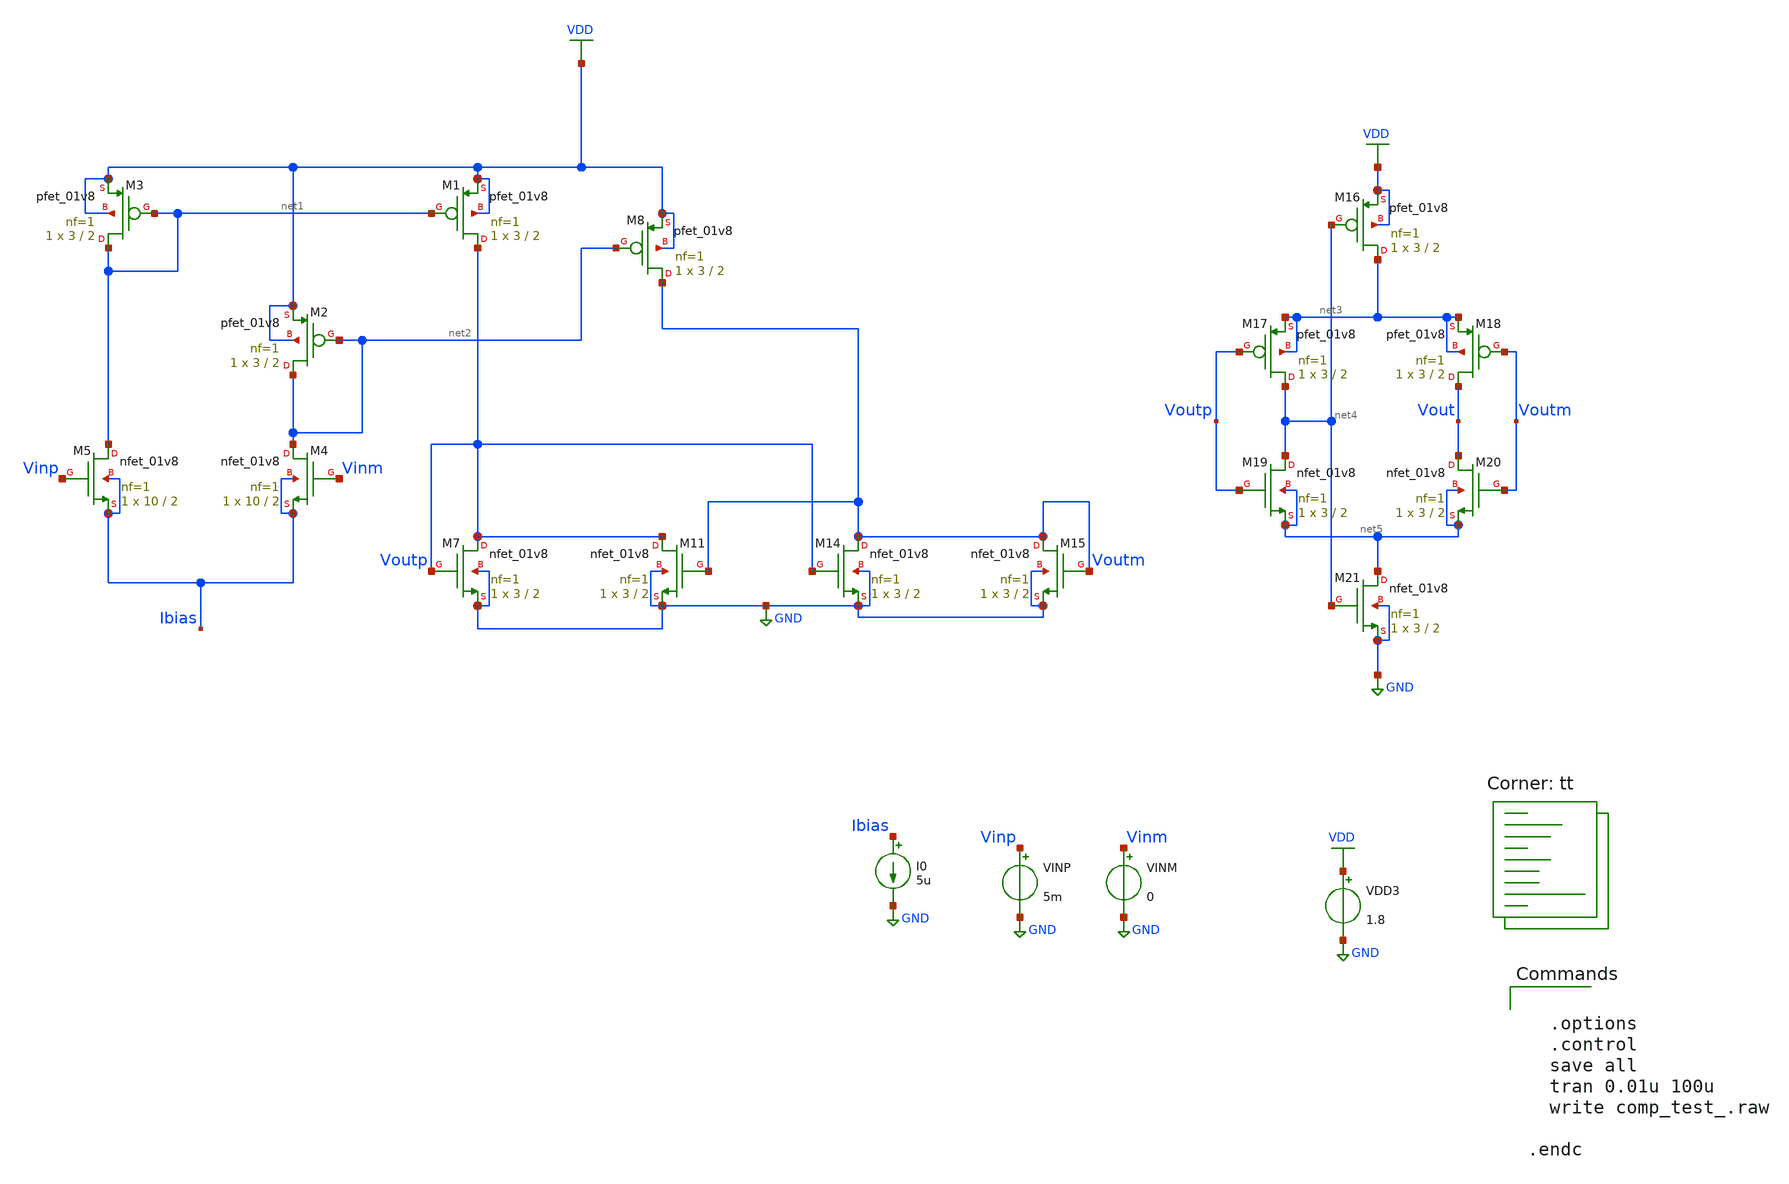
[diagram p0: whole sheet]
** sch_path: comp_test_.sch
**.subckt comp_test_
XM3 net1 net1 VDD VDD sky130_fd_pr__pfet_01v8 L=2 W=3 nf=1 ad='int((nf+1)/2) * W/nf * 0.29' as='int((nf+2)/2) * W/nf * 0.29'
+ pd='2*int((nf+1)/2) * (W/nf + 0.29)' ps='2*int((nf+2)/2) * (W/nf + 0.29)' nrd='0.29 / W' nrs='0.29 / W'
+ sa=0 sb=0 sd=0 mult=1 m=1
XM1 Voutp net1 VDD VDD sky130_fd_pr__pfet_01v8 L=2 W=3 nf=1 ad='int((nf+1)/2) * W/nf * 0.29' as='int((nf+2)/2) * W/nf * 0.29'
+ pd='2*int((nf+1)/2) * (W/nf + 0.29)' ps='2*int((nf+2)/2) * (W/nf + 0.29)' nrd='0.29 / W' nrs='0.29 / W'
+ sa=0 sb=0 sd=0 mult=1 m=1
XM2 net2 net2 VDD VDD sky130_fd_pr__pfet_01v8 L=2 W=3 nf=1 ad='int((nf+1)/2) * W/nf * 0.29' as='int((nf+2)/2) * W/nf * 0.29'
+ pd='2*int((nf+1)/2) * (W/nf + 0.29)' ps='2*int((nf+2)/2) * (W/nf + 0.29)' nrd='0.29 / W' nrs='0.29 / W'
+ sa=0 sb=0 sd=0 mult=1 m=1
XM4 net2 Vinm Ibias Ibias sky130_fd_pr__nfet_01v8 L=2 W=10 nf=1 ad='int((1 + 1)/2) * 10 / 1 * 0.29' as='int((1 + 2)/2) * 10 / 1 * 0.29'
+ pd='2*int((1 + 1)/2) * (10 / 1 + 0.29)' ps='2*int((1 + 2)/2) * (10 / 1 + 0.29)' nrd='0.29 / 10 ' nrs='0.29 / 10 '
+ sa=0 sb=0 sd=0 mult=1 m=1
XM5 net1 Vinp Ibias Ibias sky130_fd_pr__nfet_01v8 L=2 W=10 nf=1 ad='int((1 + 1)/2) * 10 / 1 * 0.29' as='int((1 + 2)/2) * 10 / 1 * 0.29'
+ pd='2*int((1 + 1)/2) * (10 / 1 + 0.29)' ps='2*int((1 + 2)/2) * (10 / 1 + 0.29)' nrd='0.29 / 10 ' nrs='0.29 / 10 '
+ sa=0 sb=0 sd=0 mult=1 m=1
XM7 Voutp Voutp GND GND sky130_fd_pr__nfet_01v8 L=2 W=3 nf=1 ad='int((1 + 1)/2) * 3 / 1 * 0.29' as='int((1 + 2)/2) * 3 / 1 * 0.29'
+ pd='2*int((1 + 1)/2) * (3 / 1 + 0.29)' ps='2*int((1 + 2)/2) * (3 / 1 + 0.29)' nrd='0.29 / 3 ' nrs='0.29 / 3 '
+ sa=0 sb=0 sd=0 mult=1 m=1
XM8 Voutm net2 VDD VDD sky130_fd_pr__pfet_01v8 L=2 W=3 nf=1 ad='int((nf+1)/2) * W/nf * 0.29' as='int((nf+2)/2) * W/nf * 0.29'
+ pd='2*int((nf+1)/2) * (W/nf + 0.29)' ps='2*int((nf+2)/2) * (W/nf + 0.29)' nrd='0.29 / W' nrs='0.29 / W'
+ sa=0 sb=0 sd=0 mult=1 m=1
XM11 Voutp Voutm GND GND sky130_fd_pr__nfet_01v8 L=2 W=3 nf=1 ad='int((1 + 1)/2) * 3 / 1 * 0.29' as='int((1 + 2)/2) * 3 / 1 * 0.29'
+ pd='2*int((1 + 1)/2) * (3 / 1 + 0.29)' ps='2*int((1 + 2)/2) * (3 / 1 + 0.29)' nrd='0.29 / 3 ' nrs='0.29 / 3 '
+ sa=0 sb=0 sd=0 mult=1 m=1
XM14 Voutm Voutp GND GND sky130_fd_pr__nfet_01v8 L=2 W=3 nf=1 ad='int((1 + 1)/2) * 3 / 1 * 0.29' as='int((1 + 2)/2) * 3 / 1 * 0.29'
+ pd='2*int((1 + 1)/2) * (3 / 1 + 0.29)' ps='2*int((1 + 2)/2) * (3 / 1 + 0.29)' nrd='0.29 / 3 ' nrs='0.29 / 3 '
+ sa=0 sb=0 sd=0 mult=1 m=1
XM15 Voutm Voutm GND GND sky130_fd_pr__nfet_01v8 L=2 W=3 nf=1 ad='int((1 + 1)/2) * 3 / 1 * 0.29' as='int((1 + 2)/2) * 3 / 1 * 0.29'
+ pd='2*int((1 + 1)/2) * (3 / 1 + 0.29)' ps='2*int((1 + 2)/2) * (3 / 1 + 0.29)' nrd='0.29 / 3 ' nrs='0.29 / 3 '
+ sa=0 sb=0 sd=0 mult=1 m=1
XM16 net3 net4 VDD VDD sky130_fd_pr__pfet_01v8 L=2 W=3 nf=1 ad='int((nf+1)/2) * W/nf * 0.29' as='int((nf+2)/2) * W/nf * 0.29'
+ pd='2*int((nf+1)/2) * (W/nf + 0.29)' ps='2*int((nf+2)/2) * (W/nf + 0.29)' nrd='0.29 / W' nrs='0.29 / W'
+ sa=0 sb=0 sd=0 mult=1 m=1
XM17 net4 Voutp net3 net3 sky130_fd_pr__pfet_01v8 L=2 W=3 nf=1 ad='int((nf+1)/2) * W/nf * 0.29' as='int((nf+2)/2) * W/nf * 0.29'
+ pd='2*int((nf+1)/2) * (W/nf + 0.29)' ps='2*int((nf+2)/2) * (W/nf + 0.29)' nrd='0.29 / W' nrs='0.29 / W'
+ sa=0 sb=0 sd=0 mult=1 m=1
XM18 Vout Voutm net3 net3 sky130_fd_pr__pfet_01v8 L=2 W=3 nf=1 ad='int((nf+1)/2) * W/nf * 0.29' as='int((nf+2)/2) * W/nf * 0.29'
+ pd='2*int((nf+1)/2) * (W/nf + 0.29)' ps='2*int((nf+2)/2) * (W/nf + 0.29)' nrd='0.29 / W' nrs='0.29 / W'
+ sa=0 sb=0 sd=0 mult=1 m=1
XM19 net4 Voutp net5 net5 sky130_fd_pr__nfet_01v8 L=2 W=3 nf=1 ad='int((1 + 1)/2) * 3 / 1 * 0.29' as='int((1 + 2)/2) * 3 / 1 * 0.29'
+ pd='2*int((1 + 1)/2) * (3 / 1 + 0.29)' ps='2*int((1 + 2)/2) * (3 / 1 + 0.29)' nrd='0.29 / 3 ' nrs='0.29 / 3 '
+ sa=0 sb=0 sd=0 mult=1 m=1
XM20 Vout Voutm net5 net5 sky130_fd_pr__nfet_01v8 L=2 W=3 nf=1 ad='int((1 + 1)/2) * 3 / 1 * 0.29' as='int((1 + 2)/2) * 3 / 1 * 0.29'
+ pd='2*int((1 + 1)/2) * (3 / 1 + 0.29)' ps='2*int((1 + 2)/2) * (3 / 1 + 0.29)' nrd='0.29 / 3 ' nrs='0.29 / 3 '
+ sa=0 sb=0 sd=0 mult=1 m=1
XM21 net5 net4 GND GND sky130_fd_pr__nfet_01v8 L=2 W=3 nf=1 ad='int((1 + 1)/2) * 3 / 1 * 0.29' as='int((1 + 2)/2) * 3 / 1 * 0.29'
+ pd='2*int((1 + 1)/2) * (3 / 1 + 0.29)' ps='2*int((1 + 2)/2) * (3 / 1 + 0.29)' nrd='0.29 / 3 ' nrs='0.29 / 3 '
+ sa=0 sb=0 sd=0 mult=1 m=1
VDD3 VDD GND 1.8
VINP Vinp GND 5m
VINM Vinm GND 0
I0 Ibias GND 5u
**** begin user architecture code


  .options
  .control
  save all
  tran 0.01u 100u
  write comp_test_.raw

.endc


.lib $::SKYWATER_MODELS/sky130.lib.spice tt
**** end user architecture code
**.ends
.GLOBAL VDD
.GLOBAL GND
.end
